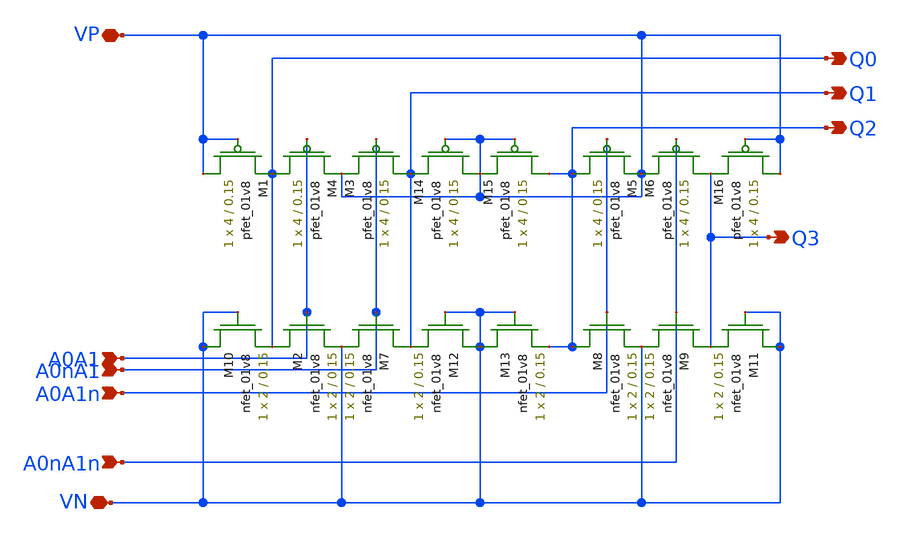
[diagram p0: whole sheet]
** sch_path: DRAM_Components/Schematic/PullUpTreeDecoder.sch
**.subckt PullUpTreeDecoder VP VN A0A1 A0nA1 A0A1n A0nA1n Q0 Q1 Q2 Q3
*.iopin VP
*.iopin VN
*.ipin A0A1
*.ipin A0nA1
*.ipin A0A1n
*.ipin A0nA1n
*.opin Q0
*.opin Q1
*.opin Q2
*.opin Q3
XM2 Q0 A0A1 VN VN sky130_fd_pr__nfet_01v8 L=0.15 W=2 nf=1 ad='int((nf+1)/2) * W/nf * 0.29' as='int((nf+2)/2) * W/nf * 0.29'
+ pd='2*int((nf+1)/2) * (W/nf + 0.29)' ps='2*int((nf+2)/2) * (W/nf + 0.29)' nrd='0.29 / W' nrs='0.29 / W'
+ sa=0 sb=0 sd=0 mult=1 m=1
XM3 Q1 A0nA1 VP VP sky130_fd_pr__pfet_01v8 L=0.15 W=4 nf=1 ad='int((nf+1)/2) * W/nf * 0.29' as='int((nf+2)/2) * W/nf * 0.29'
+ pd='2*int((nf+1)/2) * (W/nf + 0.29)' ps='2*int((nf+2)/2) * (W/nf + 0.29)' nrd='0.29 / W' nrs='0.29 / W'
+ sa=0 sb=0 sd=0 mult=1 m=1
XM4 Q0 A0A1 VP VP sky130_fd_pr__pfet_01v8 L=0.15 W=4 nf=1 ad='int((nf+1)/2) * W/nf * 0.29' as='int((nf+2)/2) * W/nf * 0.29'
+ pd='2*int((nf+1)/2) * (W/nf + 0.29)' ps='2*int((nf+2)/2) * (W/nf + 0.29)' nrd='0.29 / W' nrs='0.29 / W'
+ sa=0 sb=0 sd=0 mult=1 m=1
XM5 Q2 A0A1n VP VP sky130_fd_pr__pfet_01v8 L=0.15 W=4 nf=1 ad='int((nf+1)/2) * W/nf * 0.29' as='int((nf+2)/2) * W/nf * 0.29'
+ pd='2*int((nf+1)/2) * (W/nf + 0.29)' ps='2*int((nf+2)/2) * (W/nf + 0.29)' nrd='0.29 / W' nrs='0.29 / W'
+ sa=0 sb=0 sd=0 mult=1 m=1
XM6 Q3 A0nA1n VP VP sky130_fd_pr__pfet_01v8 L=0.15 W=4 nf=1 ad='int((nf+1)/2) * W/nf * 0.29' as='int((nf+2)/2) * W/nf * 0.29'
+ pd='2*int((nf+1)/2) * (W/nf + 0.29)' ps='2*int((nf+2)/2) * (W/nf + 0.29)' nrd='0.29 / W' nrs='0.29 / W'
+ sa=0 sb=0 sd=0 mult=1 m=1
XM7 Q1 A0nA1 VN VN sky130_fd_pr__nfet_01v8 L=0.15 W=2 nf=1 ad='int((nf+1)/2) * W/nf * 0.29' as='int((nf+2)/2) * W/nf * 0.29'
+ pd='2*int((nf+1)/2) * (W/nf + 0.29)' ps='2*int((nf+2)/2) * (W/nf + 0.29)' nrd='0.29 / W' nrs='0.29 / W'
+ sa=0 sb=0 sd=0 mult=1 m=1
XM8 Q2 A0A1n VN VN sky130_fd_pr__nfet_01v8 L=0.15 W=2 nf=1 ad='int((nf+1)/2) * W/nf * 0.29' as='int((nf+2)/2) * W/nf * 0.29'
+ pd='2*int((nf+1)/2) * (W/nf + 0.29)' ps='2*int((nf+2)/2) * (W/nf + 0.29)' nrd='0.29 / W' nrs='0.29 / W'
+ sa=0 sb=0 sd=0 mult=1 m=1
XM9 Q3 A0nA1n VN VN sky130_fd_pr__nfet_01v8 L=0.15 W=2 nf=1 ad='int((nf+1)/2) * W/nf * 0.29' as='int((nf+2)/2) * W/nf * 0.29'
+ pd='2*int((nf+1)/2) * (W/nf + 0.29)' ps='2*int((nf+2)/2) * (W/nf + 0.29)' nrd='0.29 / W' nrs='0.29 / W'
+ sa=0 sb=0 sd=0 mult=1 m=1
XM1 VP VP Q0 VP sky130_fd_pr__pfet_01v8 L=0.15 W=4 nf=1 ad='int((nf+1)/2) * W/nf * 0.29' as='int((nf+2)/2) * W/nf * 0.29'
+ pd='2*int((nf+1)/2) * (W/nf + 0.29)' ps='2*int((nf+2)/2) * (W/nf + 0.29)' nrd='0.29 / W' nrs='0.29 / W'
+ sa=0 sb=0 sd=0 mult=1 m=1
XM10 VN VN Q0 VN sky130_fd_pr__nfet_01v8 L=0.15 W=2 nf=1 ad='int((nf+1)/2) * W/nf * 0.29' as='int((nf+2)/2) * W/nf * 0.29'
+ pd='2*int((nf+1)/2) * (W/nf + 0.29)' ps='2*int((nf+2)/2) * (W/nf + 0.29)' nrd='0.29 / W' nrs='0.29 / W'
+ sa=0 sb=0 sd=0 mult=1 m=1
XM11 VN VN Q3 VN sky130_fd_pr__nfet_01v8 L=0.15 W=2 nf=1 ad='int((nf+1)/2) * W/nf * 0.29' as='int((nf+2)/2) * W/nf * 0.29'
+ pd='2*int((nf+1)/2) * (W/nf + 0.29)' ps='2*int((nf+2)/2) * (W/nf + 0.29)' nrd='0.29 / W' nrs='0.29 / W'
+ sa=0 sb=0 sd=0 mult=1 m=1
XM12 VN VN Q1 VN sky130_fd_pr__nfet_01v8 L=0.15 W=2 nf=1 ad='int((nf+1)/2) * W/nf * 0.29' as='int((nf+2)/2) * W/nf * 0.29'
+ pd='2*int((nf+1)/2) * (W/nf + 0.29)' ps='2*int((nf+2)/2) * (W/nf + 0.29)' nrd='0.29 / W' nrs='0.29 / W'
+ sa=0 sb=0 sd=0 mult=1 m=1
XM13 VN VN Q2 VN sky130_fd_pr__nfet_01v8 L=0.15 W=2 nf=1 ad='int((nf+1)/2) * W/nf * 0.29' as='int((nf+2)/2) * W/nf * 0.29'
+ pd='2*int((nf+1)/2) * (W/nf + 0.29)' ps='2*int((nf+2)/2) * (W/nf + 0.29)' nrd='0.29 / W' nrs='0.29 / W'
+ sa=0 sb=0 sd=0 mult=1 m=1
XM14 VP VP Q1 VP sky130_fd_pr__pfet_01v8 L=0.15 W=4 nf=1 ad='int((nf+1)/2) * W/nf * 0.29' as='int((nf+2)/2) * W/nf * 0.29'
+ pd='2*int((nf+1)/2) * (W/nf + 0.29)' ps='2*int((nf+2)/2) * (W/nf + 0.29)' nrd='0.29 / W' nrs='0.29 / W'
+ sa=0 sb=0 sd=0 mult=1 m=1
XM15 Q2 VP VP VP sky130_fd_pr__pfet_01v8 L=0.15 W=4 nf=1 ad='int((nf+1)/2) * W/nf * 0.29' as='int((nf+2)/2) * W/nf * 0.29'
+ pd='2*int((nf+1)/2) * (W/nf + 0.29)' ps='2*int((nf+2)/2) * (W/nf + 0.29)' nrd='0.29 / W' nrs='0.29 / W'
+ sa=0 sb=0 sd=0 mult=1 m=1
XM16 VP VP Q3 VP sky130_fd_pr__pfet_01v8 L=0.15 W=4 nf=1 ad='int((nf+1)/2) * W/nf * 0.29' as='int((nf+2)/2) * W/nf * 0.29'
+ pd='2*int((nf+1)/2) * (W/nf + 0.29)' ps='2*int((nf+2)/2) * (W/nf + 0.29)' nrd='0.29 / W' nrs='0.29 / W'
+ sa=0 sb=0 sd=0 mult=1 m=1
**.ends
.end
